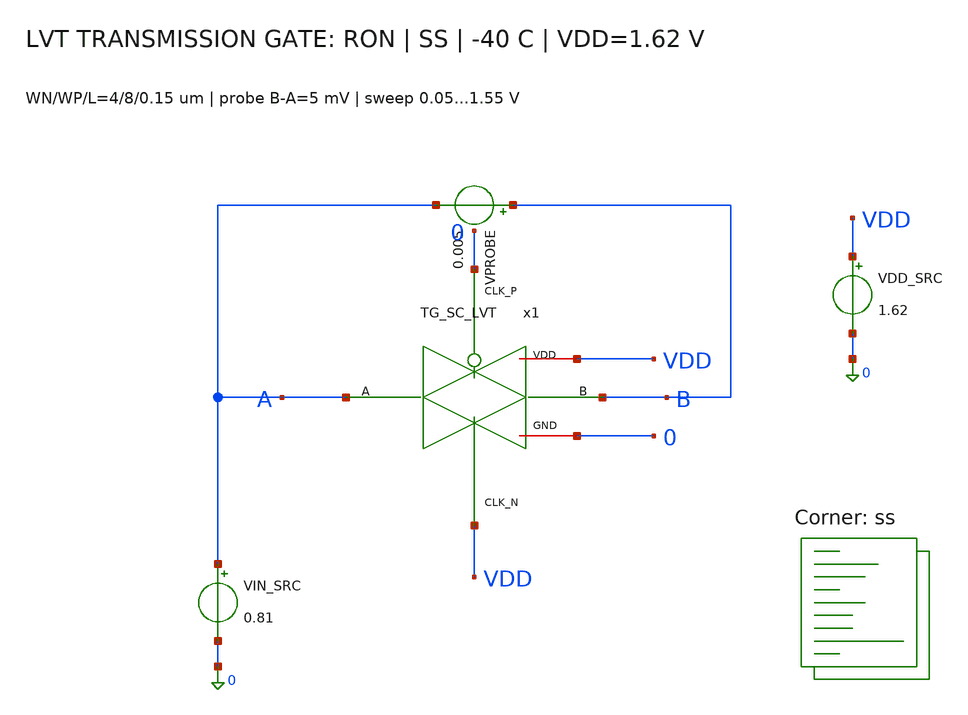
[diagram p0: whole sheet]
** sch_path: blocks/05_Switch_Network/sim/tb_5B_ron_lvt.sch
**.subckt tb_5B_ron_lvt
VPROBE B A 0.005
.save i(vprobe)
VIN_SRC A 0 0.81
VDD_SRC VDD 0 1.62
x1 A B 0 VDD VDD 0 TG_SC_LVT
**** begin user architecture code
.lib $::SKYWATER_MODELS/sky130.lib.spice ss


.option scale=1e-6 reltol=1e-5 abstol=1e-14 vntol=1e-8
.temp -40
.control
save all
set wr_singlescale
set wr_vecnames
set numdgt=15
dc VIN_SRC 0.05 1.55 0.005
let RON=abs((v(B)-v(A))/i(VPROBE))
meas dc RON_MIN MIN RON
meas dc RON_MAX MAX RON
meas dc RON_060 FIND RON AT=0.6
meas dc RON_081 FIND RON AT=0.81
meas dc RON_089 FIND RON AT=0.89
meas dc RON_090 FIND RON AT=0.9
meas dc RON_120 FIND RON AT=1.2
wrdata ron_tg_lvt_ss_1p62_m40.dat v(A) v(B) i(VPROBE) RON
plot RON
.endc


**** end user architecture code
**.ends

* expanding   symbol:  blocks/05_Switch_Network/xschem/TG_SC_LVT.sym # of pins=6
** sym_path: blocks/05_Switch_Network/xschem/TG_SC_LVT.sym
** sch_path: blocks/05_Switch_Network/xschem/TG_SC_LVT.sch
.subckt TG_SC_LVT A B CLK_P CLK_N VDD GND
*.iopin A
*.iopin B
*.ipin CLK_P
*.ipin CLK_N
*.iopin VDD
*.iopin GND
XMP A CLK_P B VDD sky130_fd_pr__pfet_01v8_lvt L=0.35 W=8 nf=1 ad='int((1 + 1)/2) * 8 / 1 * 0.29' as='int((1 + 2)/2) * 8 / 1 * 0.29'
+ pd='2*int((1 + 1)/2) * (8 / 1 + 0.29)' ps='2*int((1 + 2)/2) * (8 / 1 + 0.29)' nrd='0.29 / 8 ' nrs='0.29 / 8 '
+ sa=0 sb=0 sd=0 mult=1
XMN A CLK_N B GND sky130_fd_pr__nfet_01v8_lvt L=0.15 W=4 nf=1 ad='int((1 + 1)/2) * 4 / 1 * 0.29' as='int((1 + 2)/2) * 4 / 1 * 0.29'
+ pd='2*int((1 + 1)/2) * (4 / 1 + 0.29)' ps='2*int((1 + 2)/2) * (4 / 1 + 0.29)' nrd='0.29 / 4 ' nrs='0.29 / 4 '
+ sa=0 sb=0 sd=0 mult=1
.ends

.end
